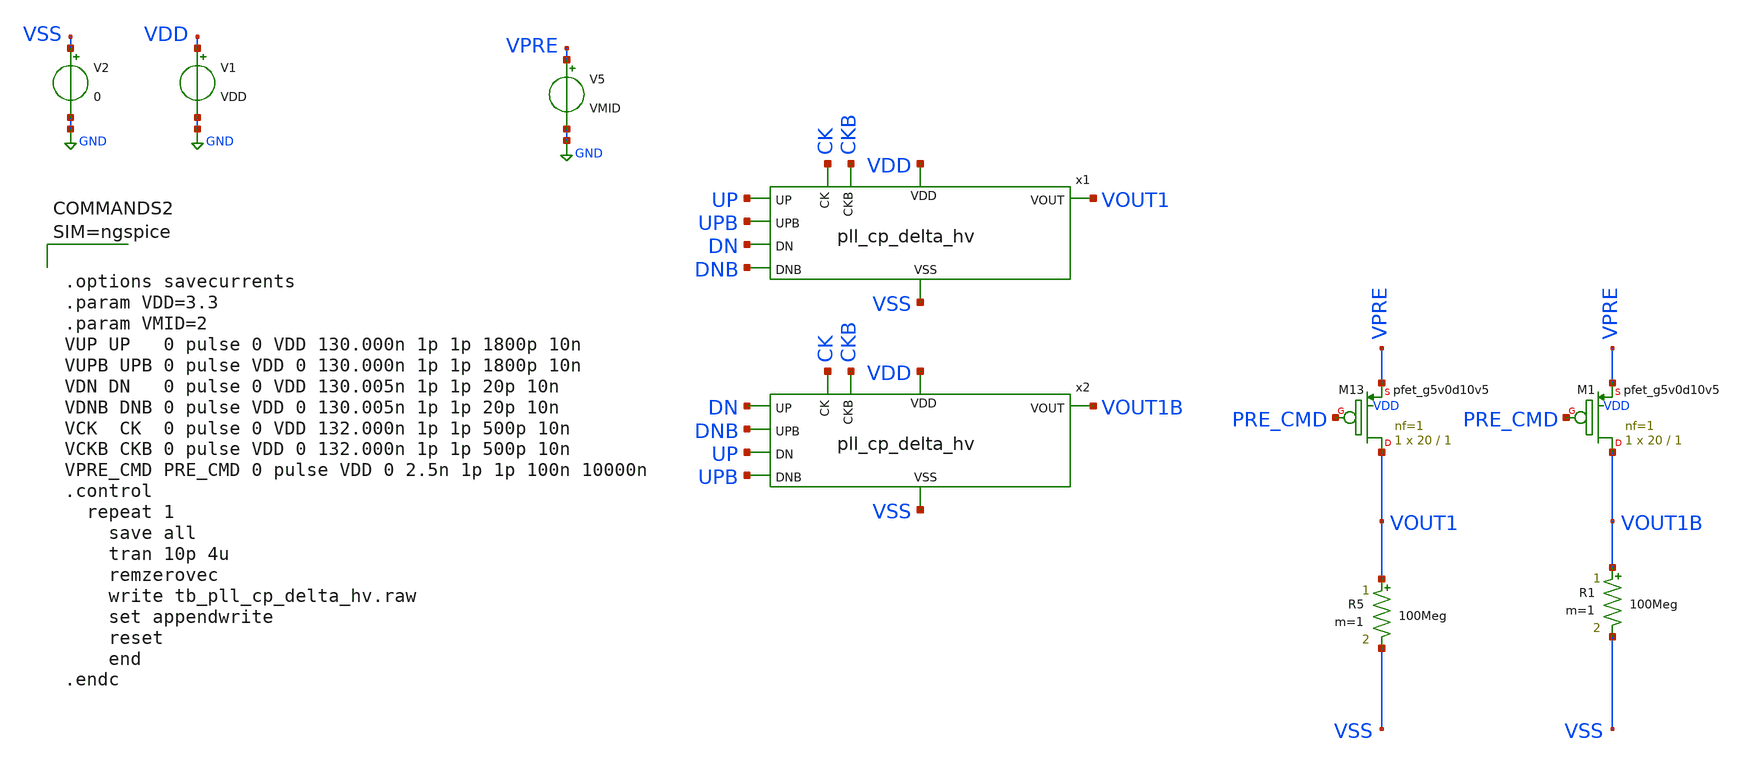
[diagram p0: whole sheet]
** sch_path: xschem/tb_pll_cp_delta_hv.sch
**.subckt tb_pll_cp_delta_hv
V1 VDD GND VDD
V2 VSS GND 0
V5 VPRE GND VMID
x1 VDD UP DN VOUT1 VSS UPB DNB CK CKB pll_cp_delta_hv
R5 VOUT1 VSS 100Meg m=1
R1 VOUT1B VSS 100Meg m=1
x2 VDD DN UP VOUT1B VSS DNB UPB CK CKB pll_cp_delta_hv
XM13 VOUT1 PRE_CMD VPRE VDD sky130_fd_pr__pfet_g5v0d10v5 L=1 W=20 nf=1 ad='int((nf+1)/2) * W/nf * 0.29'
+ as='int((nf+2)/2) * W/nf * 0.29' pd='2*int((nf+1)/2) * (W/nf + 0.29)' ps='2*int((nf+2)/2) * (W/nf + 0.29)'
+ nrd='0.29 / W' nrs='0.29 / W' sa=0 sb=0 sd=0 mult=1 m=1
XM1 VOUT1B PRE_CMD VPRE VDD sky130_fd_pr__pfet_g5v0d10v5 L=1 W=20 nf=1 ad='int((nf+1)/2) * W/nf * 0.29'
+ as='int((nf+2)/2) * W/nf * 0.29' pd='2*int((nf+1)/2) * (W/nf + 0.29)' ps='2*int((nf+2)/2) * (W/nf + 0.29)'
+ nrd='0.29 / W' nrs='0.29 / W' sa=0 sb=0 sd=0 mult=1 m=1
**** begin user architecture code

** opencircuitdesign pdks install
.lib $::SKYWATER_MODELS/sky130.lib.spice tt





.options savecurrents
.param VDD=3.3
.param VMID=2
VUP UP   0 pulse 0 VDD 130.000n 1p 1p 1800p 10n
VUPB UPB 0 pulse VDD 0 130.000n 1p 1p 1800p 10n
VDN DN   0 pulse 0 VDD 130.005n 1p 1p 20p 10n
VDNB DNB 0 pulse VDD 0 130.005n 1p 1p 20p 10n
VCK  CK  0 pulse 0 VDD 132.000n 1p 1p 500p 10n
VCKB CKB 0 pulse VDD 0 132.000n 1p 1p 500p 10n
VPRE_CMD PRE_CMD 0 pulse VDD 0 2.5n 1p 1p 100n 10000n
.control
  repeat 1
    save all
    tran 10p 4u
    remzerovec
    write tb_pll_cp_delta_hv.raw
    set appendwrite
    reset
    end
.endc



**** end user architecture code
**.ends

* expanding   symbol:  pll_cp_delta_hv.sym # of pins=9
** sym_path: xschem/pll_cp_delta_hv.sym
** sch_path: xschem/pll_cp_delta_hv.sch
.subckt pll_cp_delta_hv VDD UP DN VOUT VSS UPB DNB CK CKB
*.opin VOUT
*.ipin VSS
*.ipin UP
*.ipin DNB
*.ipin CK
*.ipin CKB
*.ipin VDD
*.ipin DN
*.ipin UPB
*.ipin CK
vibias net3 net10 0
.save i(vibias)
XM16 net6 UPB VDD VDD sky130_fd_pr__pfet_g5v0d10v5 L=1 W=3 nf=1 ad='int((nf+1)/2) * W/nf * 0.29' as='int((nf+2)/2) * W/nf * 0.29'
+ pd='2*int((nf+1)/2) * (W/nf + 0.29)' ps='2*int((nf+2)/2) * (W/nf + 0.29)' nrd='0.29 / W' nrs='0.29 / W'
+ sa=0 sb=0 sd=0 mult=1 m=1
XM13 net2 VSS VDD VDD sky130_fd_pr__pfet_g5v0d10v5 L=1 W=2 nf=1 ad='int((nf+1)/2) * W/nf * 0.29' as='int((nf+2)/2) * W/nf * 0.29'
+ pd='2*int((nf+1)/2) * (W/nf + 0.29)' ps='2*int((nf+2)/2) * (W/nf + 0.29)' nrd='0.29 / W' nrs='0.29 / W'
+ sa=0 sb=0 sd=0 mult=1 m=1
XM14 net3 net3 net2 VDD sky130_fd_pr__pfet_g5v0d10v5 L=1 W=2 nf=1 ad='int((nf+1)/2) * W/nf * 0.29' as='int((nf+2)/2) * W/nf * 0.29'
+ pd='2*int((nf+1)/2) * (W/nf + 0.29)' ps='2*int((nf+2)/2) * (W/nf + 0.29)' nrd='0.29 / W' nrs='0.29 / W'
+ sa=0 sb=0 sd=0 mult=1 m=1
I0 VDD net4 10u
XM11 net1 VDD VSS VSS sky130_fd_pr__nfet_g5v0d10v5 L=1 W=2 nf=1 ad='int((nf+1)/2) * W/nf * 0.29' as='int((nf+2)/2) * W/nf * 0.29'
+ pd='2*int((nf+1)/2) * (W/nf + 0.29)' ps='2*int((nf+2)/2) * (W/nf + 0.29)' nrd='0.29 / W' nrs='0.29 / W'
+ sa=0 sb=0 sd=0 mult=1 m=1
XM17 net4 net4 net1 VSS sky130_fd_pr__nfet_g5v0d10v5 L=1 W=2 nf=1 ad='int((nf+1)/2) * W/nf * 0.29' as='int((nf+2)/2) * W/nf * 0.29'
+ pd='2*int((nf+1)/2) * (W/nf + 0.29)' ps='2*int((nf+2)/2) * (W/nf + 0.29)' nrd='0.29 / W' nrs='0.29 / W'
+ sa=0 sb=0 sd=0 mult=1 m=1
XM15 net5 VDD VSS VSS sky130_fd_pr__nfet_g5v0d10v5 L=1 W=2 nf=1 ad='int((nf+1)/2) * W/nf * 0.29' as='int((nf+2)/2) * W/nf * 0.29'
+ pd='2*int((nf+1)/2) * (W/nf + 0.29)' ps='2*int((nf+2)/2) * (W/nf + 0.29)' nrd='0.29 / W' nrs='0.29 / W'
+ sa=0 sb=0 sd=0 mult=1 m=1
XM18 net10 net4 net5 VSS sky130_fd_pr__nfet_g5v0d10v5 L=1 W=2 nf=1 ad='int((nf+1)/2) * W/nf * 0.29' as='int((nf+2)/2) * W/nf * 0.29'
+ pd='2*int((nf+1)/2) * (W/nf + 0.29)' ps='2*int((nf+2)/2) * (W/nf + 0.29)' nrd='0.29 / W' nrs='0.29 / W'
+ sa=0 sb=0 sd=0 mult=1 m=1
XM6 net8 DN VSS VSS sky130_fd_pr__nfet_g5v0d10v5 L=1 W=2 nf=1 ad='int((nf+1)/2) * W/nf * 0.29' as='int((nf+2)/2) * W/nf * 0.29'
+ pd='2*int((nf+1)/2) * (W/nf + 0.29)' ps='2*int((nf+2)/2) * (W/nf + 0.29)' nrd='0.29 / W' nrs='0.29 / W'
+ sa=0 sb=0 sd=0 mult=1 m=1
XM19 net9 net4 net8 VSS sky130_fd_pr__nfet_g5v0d10v5 L=1 W=2 nf=1 ad='int((nf+1)/2) * W/nf * 0.29' as='int((nf+2)/2) * W/nf * 0.29'
+ pd='2*int((nf+1)/2) * (W/nf + 0.29)' ps='2*int((nf+2)/2) * (W/nf + 0.29)' nrd='0.29 / W' nrs='0.29 / W'
+ sa=0 sb=0 sd=0 mult=1 m=1
XM4 net11 net3 net6 VDD sky130_fd_pr__pfet_g5v0d10v5 L=1 W=3 nf=1 ad='int((nf+1)/2) * W/nf * 0.29' as='int((nf+2)/2) * W/nf * 0.29'
+ pd='2*int((nf+1)/2) * (W/nf + 0.29)' ps='2*int((nf+2)/2) * (W/nf + 0.29)' nrd='0.29 / W' nrs='0.29 / W'
+ sa=0 sb=0 sd=0 mult=1 m=1
viup net11 VCAP 0
.save i(viup)
vidown VCAP net9 0
.save i(vidown)
XC3 VCAP VOUT sky130_fd_pr__cap_mim_m3_1 W=1 L=2 MF=1 m=1
XM3 VCAP CKB VOUT VDD sky130_fd_pr__pfet_01v8_lvt L=0.5 W=1 nf=1 ad='int((nf+1)/2) * W/nf * 0.29' as='int((nf+2)/2) * W/nf * 0.29'
+ pd='2*int((nf+1)/2) * (W/nf + 0.29)' ps='2*int((nf+2)/2) * (W/nf + 0.29)' nrd='0.29 / W' nrs='0.29 / W'
+ sa=0 sb=0 sd=0 mult=1 m=1
XM5 VCAP CK VOUT VSS sky130_fd_pr__nfet_01v8_lvt L=0.25 W=0.45 nf=1 ad='int((nf+1)/2) * W/nf * 0.29'
+ as='int((nf+2)/2) * W/nf * 0.29' pd='2*int((nf+1)/2) * (W/nf + 0.29)' ps='2*int((nf+2)/2) * (W/nf + 0.29)'
+ nrd='0.29 / W' nrs='0.29 / W' sa=0 sb=0 sd=0 mult=1 m=1
XC2 VOUT VSS sky130_fd_pr__cap_mim_m3_1 W=50 L=50 MF=1 m=1
XR1 net7 VOUT net12 sky130_fd_pr__res_xhigh_po_0p69 L=1 mult=1 m=1
.ends

.GLOBAL GND
.end
